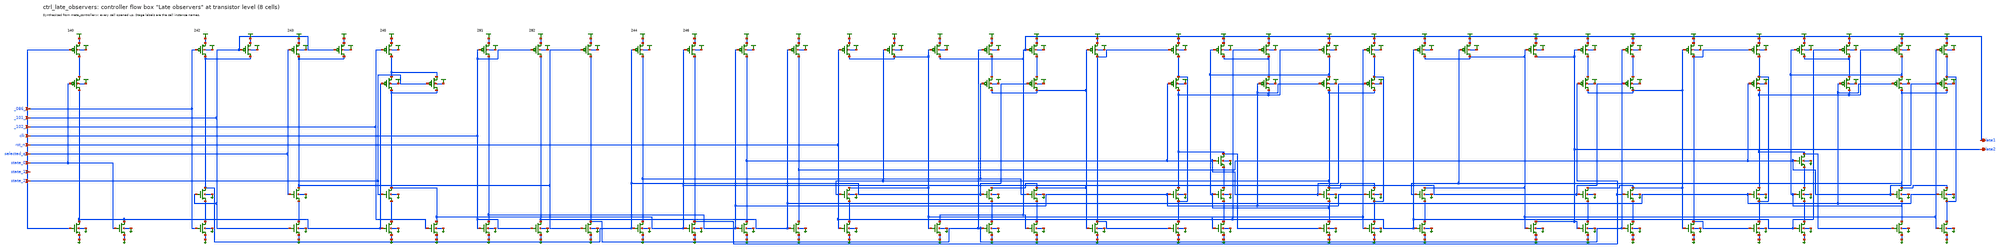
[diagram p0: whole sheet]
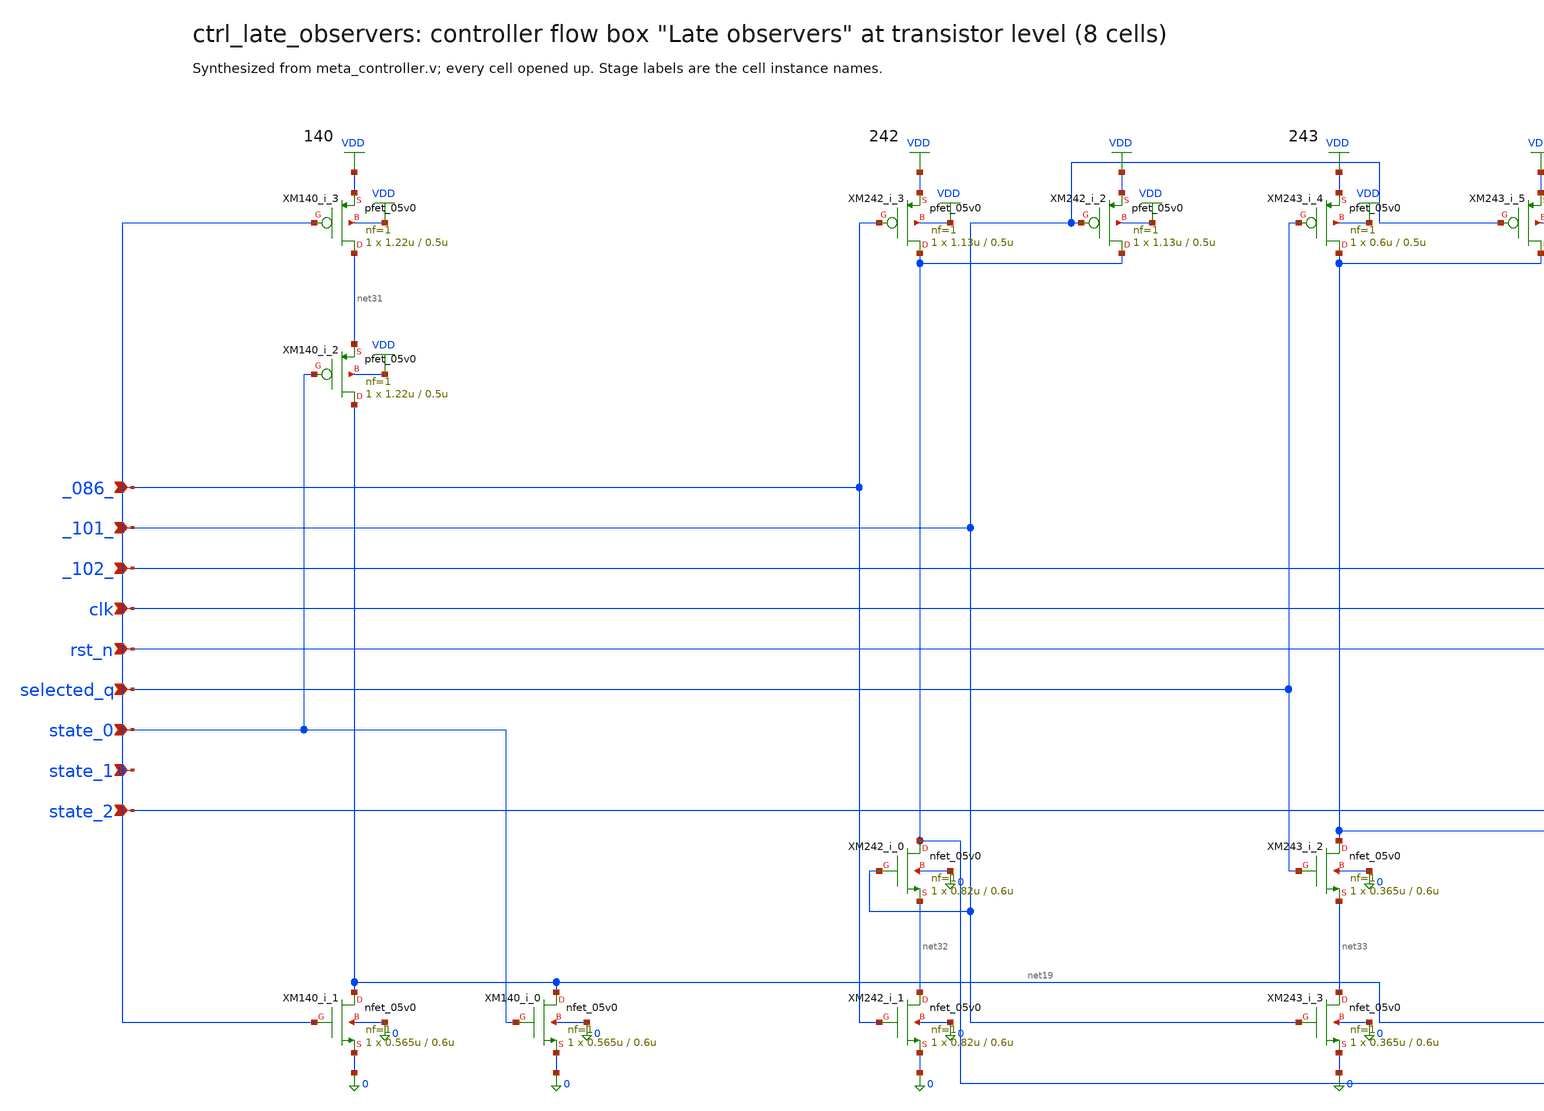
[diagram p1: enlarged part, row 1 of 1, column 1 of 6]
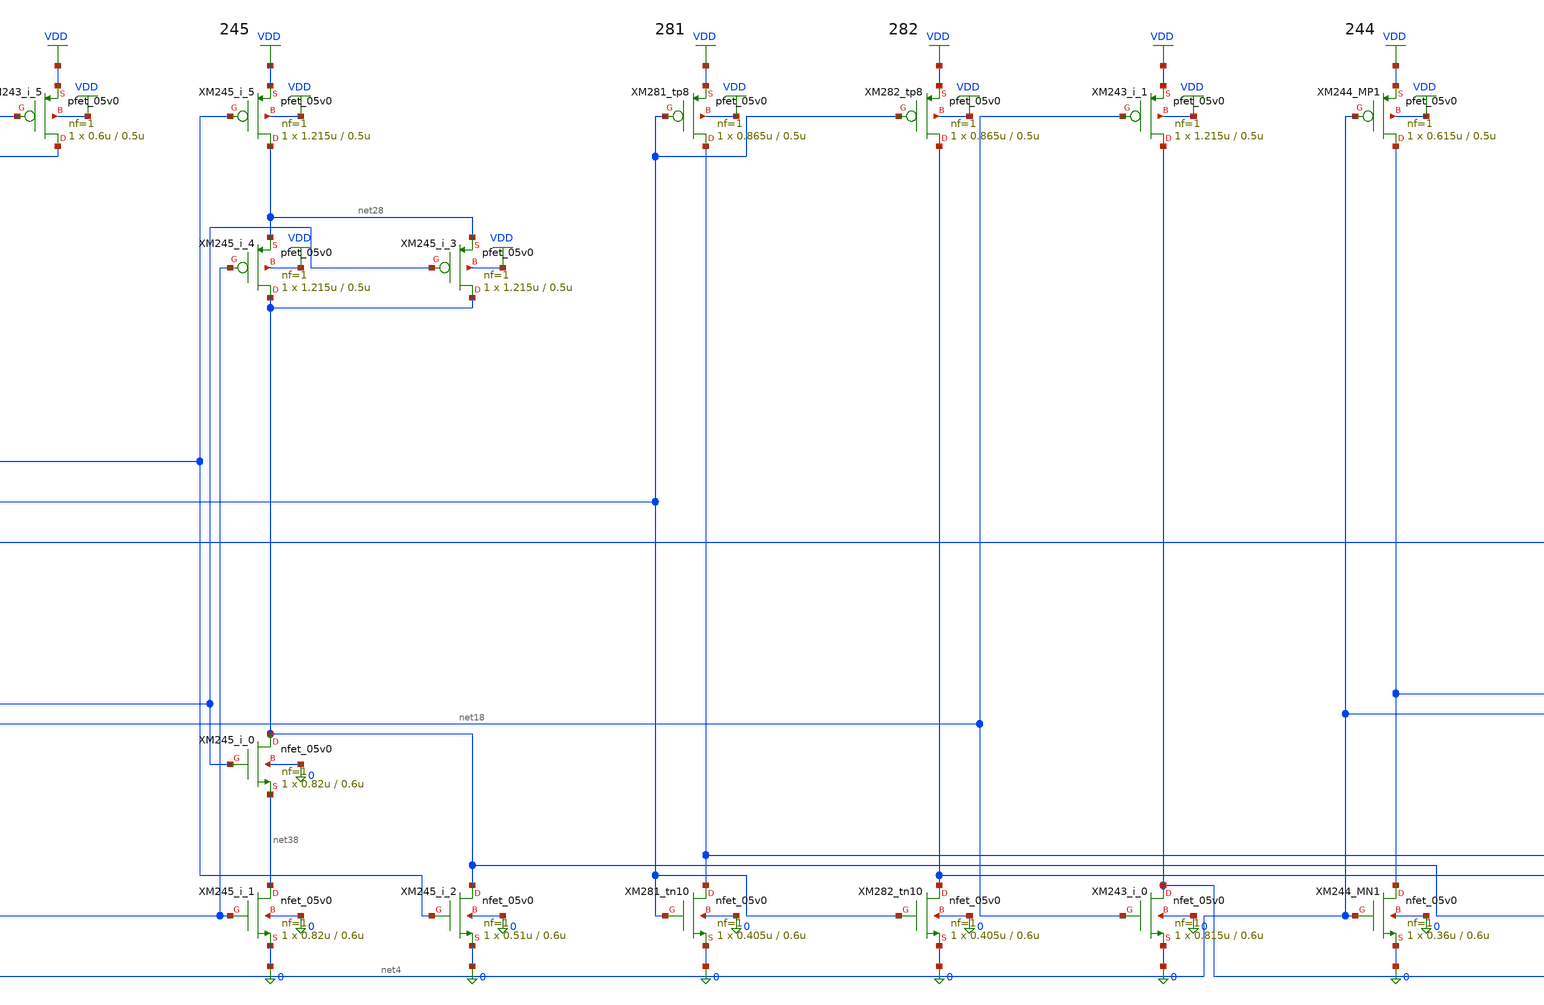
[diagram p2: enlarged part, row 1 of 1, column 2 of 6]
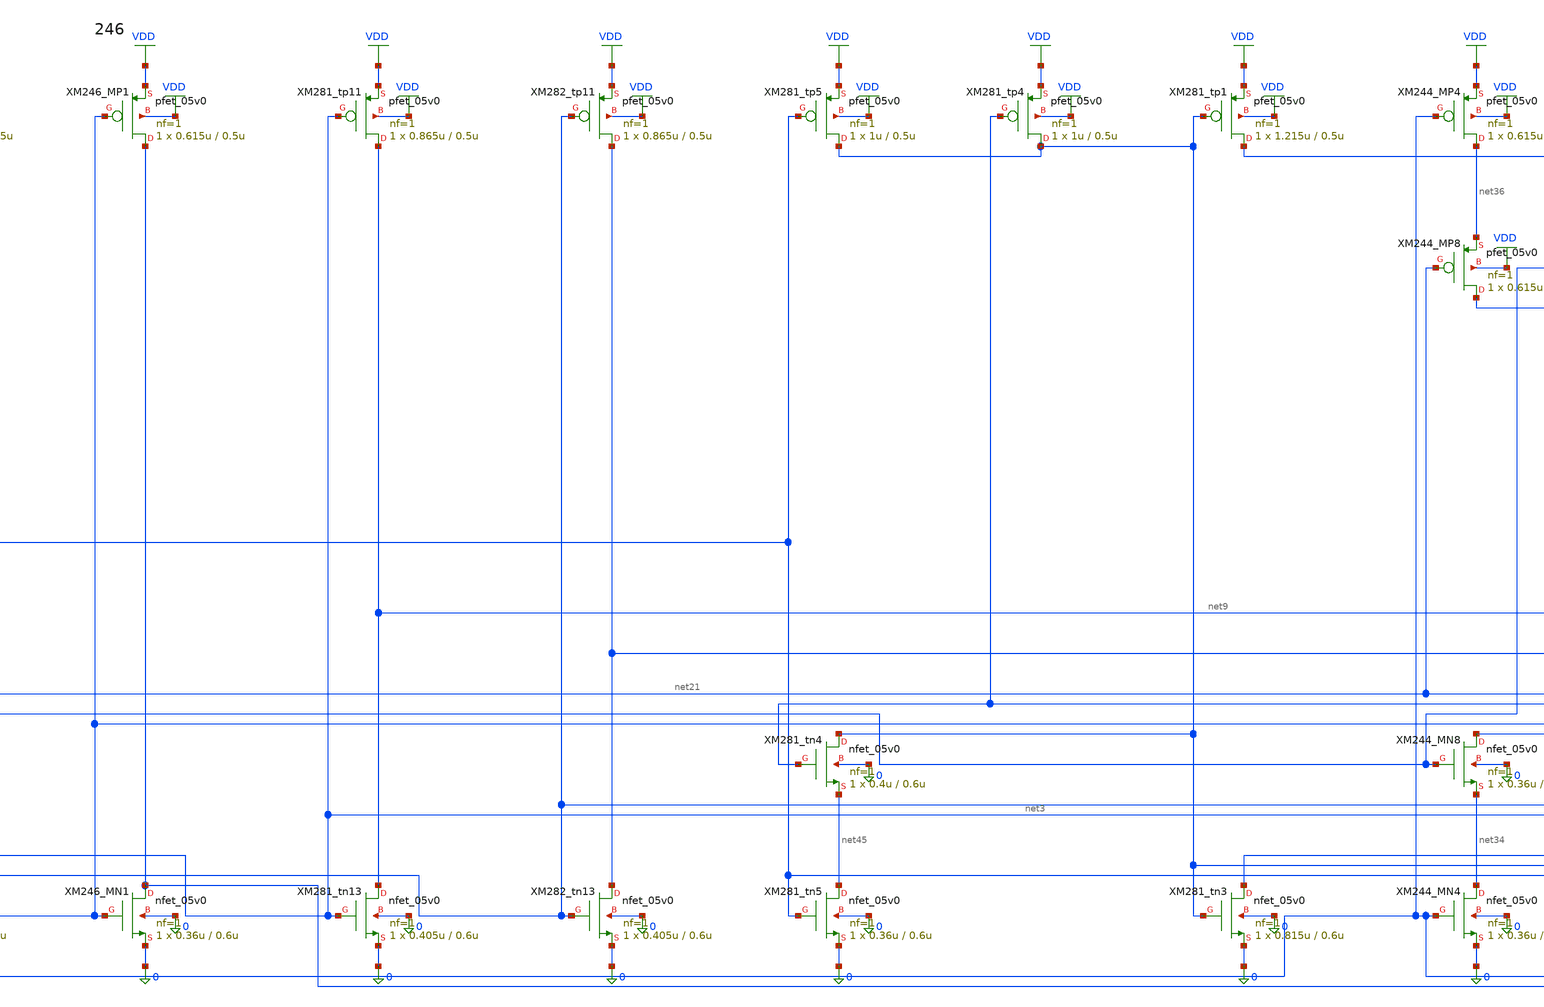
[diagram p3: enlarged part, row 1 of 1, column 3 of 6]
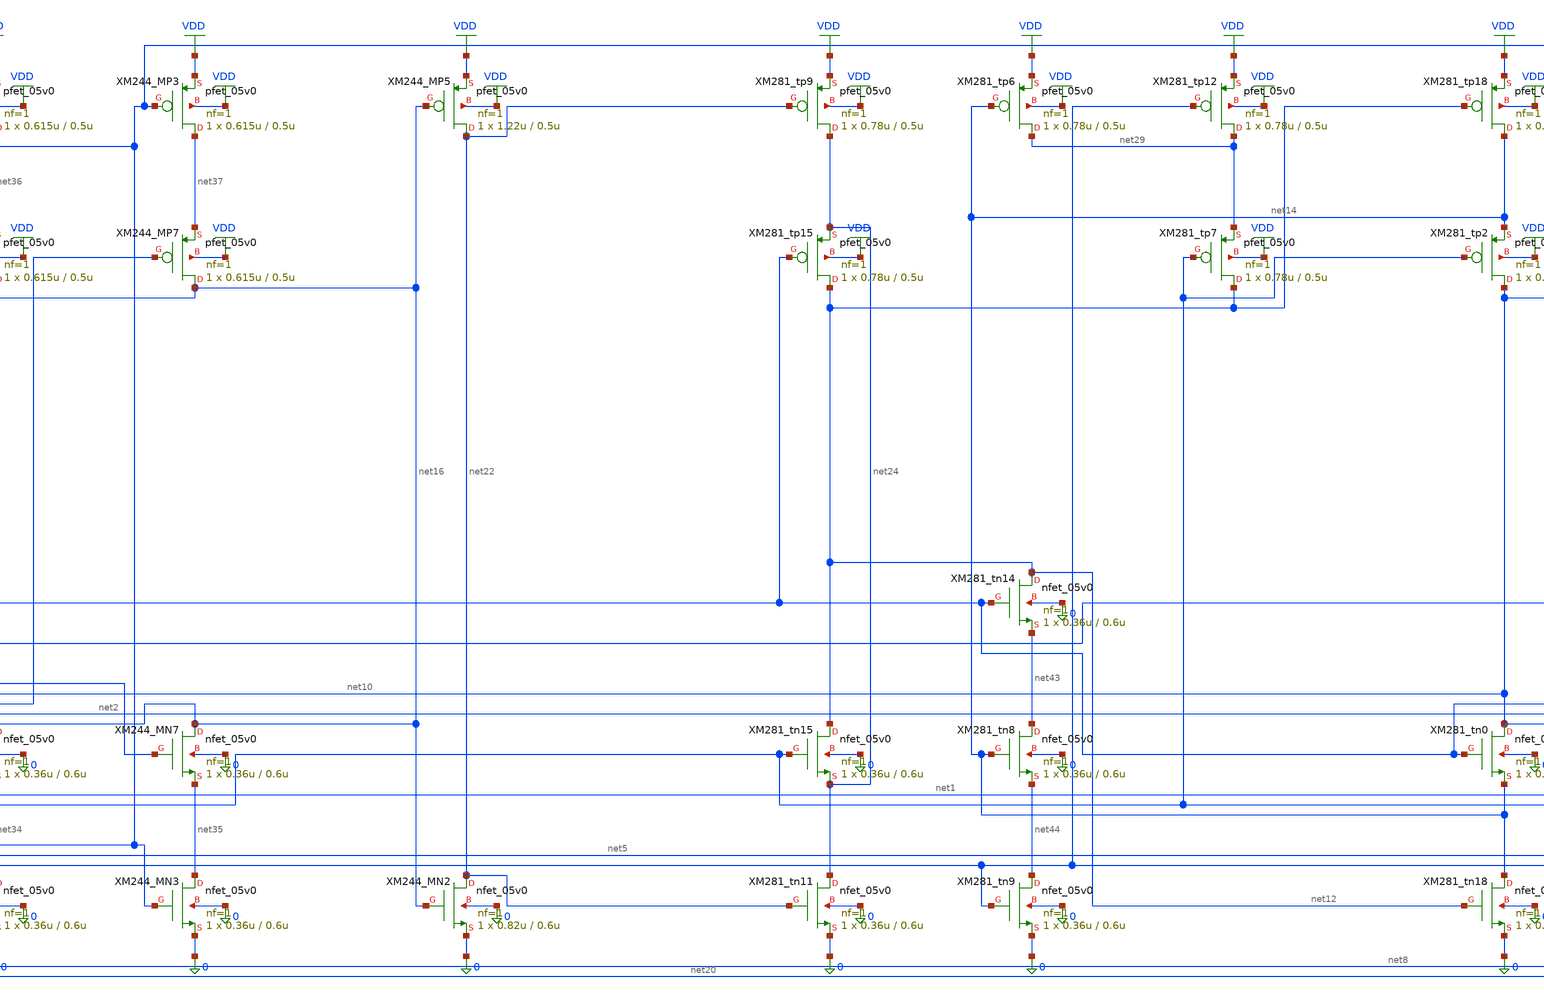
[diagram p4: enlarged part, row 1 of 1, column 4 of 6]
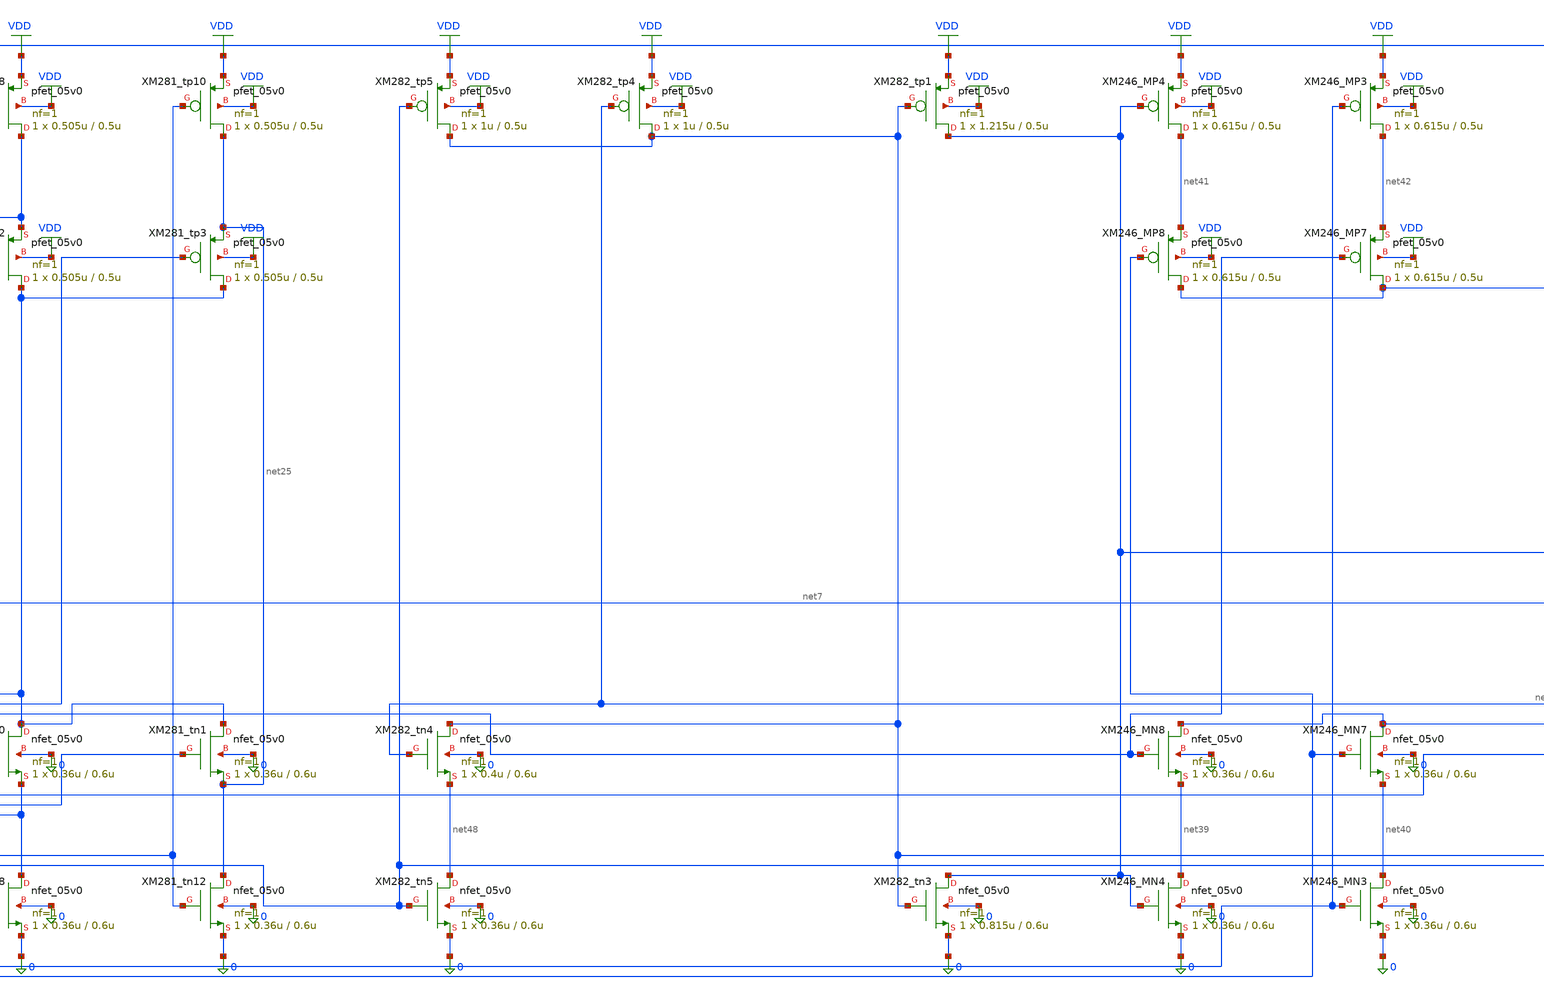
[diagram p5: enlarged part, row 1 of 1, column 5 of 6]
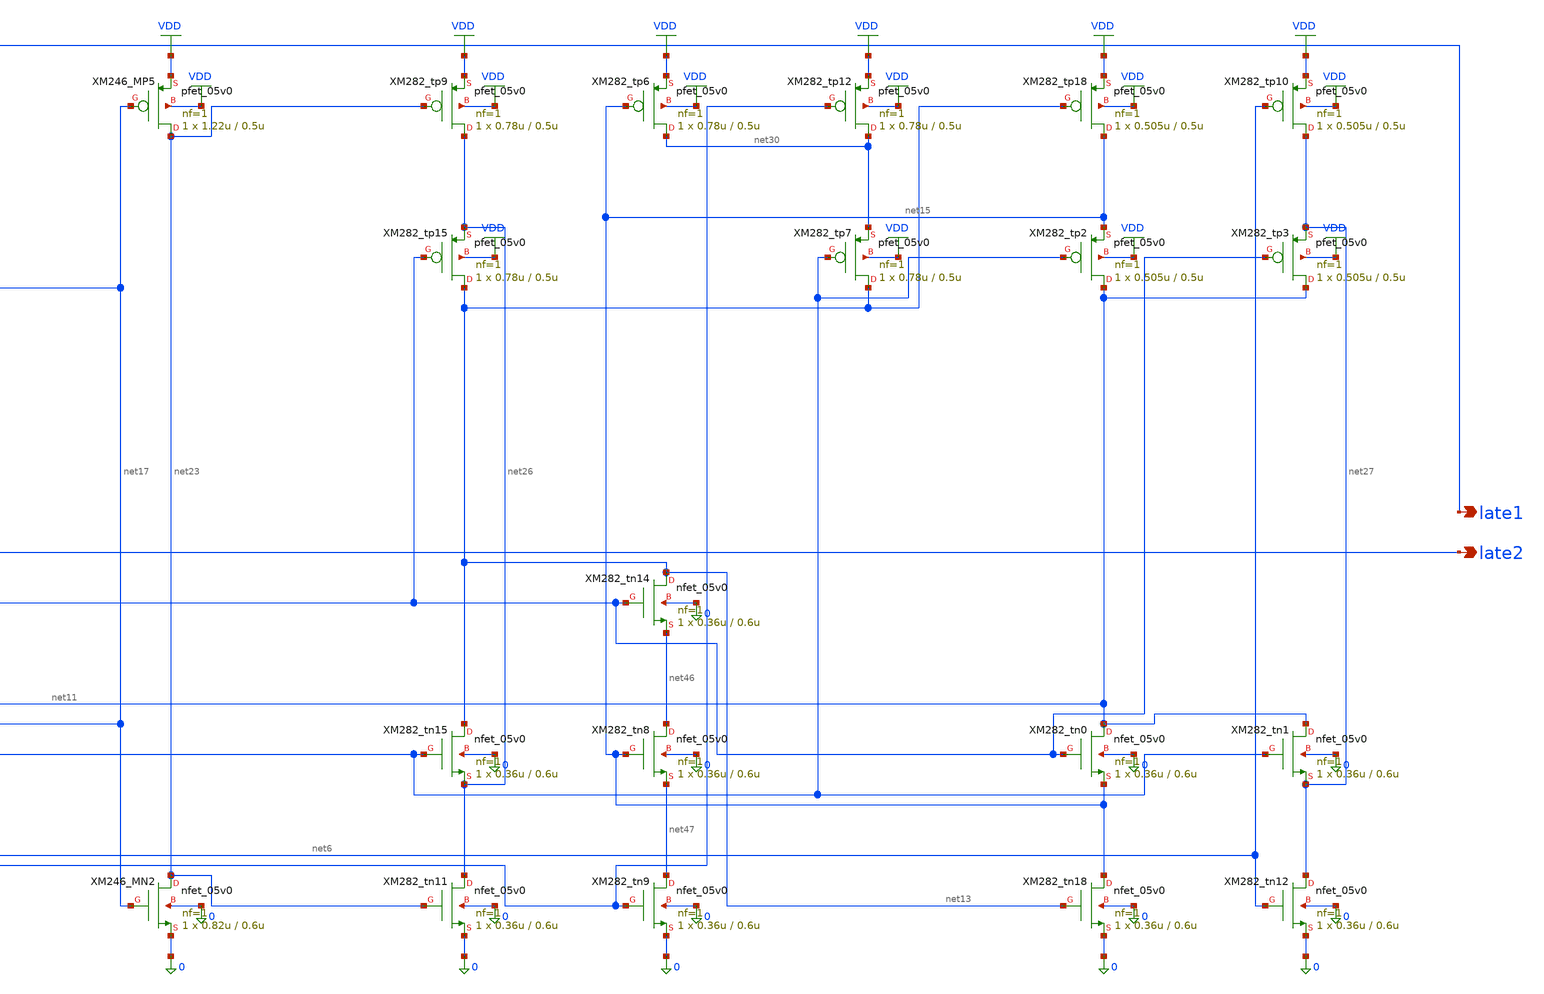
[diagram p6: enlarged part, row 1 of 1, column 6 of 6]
** sch_path: xschem/flat/ctrl_late_observers.sch
**.subckt ctrl_late_observers _086_ _101_ _102_ clk rst_n selected_q state_0 state_1 state_2 late1
*+ late2
*.ipin _086_
*.ipin _101_
*.ipin _102_
*.ipin clk
*.ipin rst_n
*.ipin selected_q
*.ipin state_0
*.ipin state_1
*.ipin state_2
*.opin late1
*.opin late2
XM140_i_1 net19 state_1 0 0 nfet_05v0 L=0.6u W=0.565u nf=1 ad=2.825e-13 as=2.825e-13 pd=2.13e-06
+ ps=2.13e-06 nrd=0 nrs=0 sa=0 sb=0 sd=0 m=1
XM140_i_0 net19 state_0 0 0 nfet_05v0 L=0.6u W=0.565u nf=1 ad=2.825e-13 as=2.825e-13 pd=2.13e-06
+ ps=2.13e-06 nrd=0 nrs=0 sa=0 sb=0 sd=0 m=1
XM140_i_3 net31 state_1 VDD VDD pfet_05v0 L=0.5u W=1.22u nf=1 ad=6.1e-13 as=6.1e-13 pd=3.44e-06
+ ps=3.44e-06 nrd=0 nrs=0 sa=0 sb=0 sd=0 m=1
XM140_i_2 net19 state_0 net31 VDD pfet_05v0 L=0.5u W=1.22u nf=1 ad=6.1e-13 as=6.1e-13 pd=3.44e-06
+ ps=3.44e-06 nrd=0 nrs=0 sa=0 sb=0 sd=0 m=1
XM242_i_1 net32 _086_ 0 0 nfet_05v0 L=0.6u W=0.82u nf=1 ad=4.1e-13 as=4.1e-13 pd=2.64e-06
+ ps=2.64e-06 nrd=0 nrs=0 sa=0 sb=0 sd=0 m=1
XM242_i_0 net4 _101_ net32 0 nfet_05v0 L=0.6u W=0.82u nf=1 ad=4.1e-13 as=4.1e-13 pd=2.64e-06
+ ps=2.64e-06 nrd=0 nrs=0 sa=0 sb=0 sd=0 m=1
XM242_i_3 net4 _086_ VDD VDD pfet_05v0 L=0.5u W=1.13u nf=1 ad=5.65e-13 as=5.65e-13 pd=3.26e-06
+ ps=3.26e-06 nrd=0 nrs=0 sa=0 sb=0 sd=0 m=1
XM242_i_2 net4 _101_ VDD VDD pfet_05v0 L=0.5u W=1.13u nf=1 ad=5.65e-13 as=5.65e-13 pd=3.26e-06
+ ps=3.26e-06 nrd=0 nrs=0 sa=0 sb=0 sd=0 m=1
XM243_i_2 net18 selected_q net33 0 nfet_05v0 L=0.6u W=0.365u nf=1 ad=1.825e-13 as=1.825e-13
+ pd=1.73e-06 ps=1.73e-06 nrd=0 nrs=0 sa=0 sb=0 sd=0 m=1
XM243_i_3 net33 _101_ 0 0 nfet_05v0 L=0.6u W=0.365u nf=1 ad=1.825e-13 as=1.825e-13 pd=1.73e-06
+ ps=1.73e-06 nrd=0 nrs=0 sa=0 sb=0 sd=0 m=1
XM243_i_0 net8 net18 0 0 nfet_05v0 L=0.6u W=0.815u nf=1 ad=4.075e-13 as=4.075e-13 pd=2.63e-06
+ ps=2.63e-06 nrd=0 nrs=0 sa=0 sb=0 sd=0 m=1
XM243_i_4 net18 selected_q VDD VDD pfet_05v0 L=0.5u W=0.6u nf=1 ad=3e-13 as=3e-13 pd=2.2e-06
+ ps=2.2e-06 nrd=0 nrs=0 sa=0 sb=0 sd=0 m=1
XM243_i_5 net18 _101_ VDD VDD pfet_05v0 L=0.5u W=0.6u nf=1 ad=3e-13 as=3e-13 pd=2.2e-06 ps=2.2e-06
+ nrd=0 nrs=0 sa=0 sb=0 sd=0 m=1
XM243_i_1 net8 net18 VDD VDD pfet_05v0 L=0.5u W=1.215u nf=1 ad=6.075e-13 as=6.075e-13 pd=3.43e-06
+ ps=3.43e-06 nrd=0 nrs=0 sa=0 sb=0 sd=0 m=1
XM244_MN2 net22 net16 0 0 nfet_05v0 L=0.6u W=0.82u nf=1 ad=4.1e-13 as=4.1e-13 pd=2.64e-06
+ ps=2.64e-06 nrd=0 nrs=0 sa=0 sb=0 sd=0 m=1
XM244_MN4 net34 net8 0 0 nfet_05v0 L=0.6u W=0.36u nf=1 ad=1.8e-13 as=1.8e-13 pd=1.72e-06 ps=1.72e-06
+ nrd=0 nrs=0 sa=0 sb=0 sd=0 m=1
XM244_MN8 net16 net4 net34 0 nfet_05v0 L=0.6u W=0.36u nf=1 ad=1.8e-13 as=1.8e-13 pd=1.72e-06
+ ps=1.72e-06 nrd=0 nrs=0 sa=0 sb=0 sd=0 m=1
XM244_MN7 net16 net21 net35 0 nfet_05v0 L=0.6u W=0.36u nf=1 ad=1.8e-13 as=1.8e-13 pd=1.72e-06
+ ps=1.72e-06 nrd=0 nrs=0 sa=0 sb=0 sd=0 m=1
XM244_MN3 net35 late1 0 0 nfet_05v0 L=0.6u W=0.36u nf=1 ad=1.8e-13 as=1.8e-13 pd=1.72e-06
+ ps=1.72e-06 nrd=0 nrs=0 sa=0 sb=0 sd=0 m=1
XM244_MN1 net21 net4 0 0 nfet_05v0 L=0.6u W=0.36u nf=1 ad=1.8e-13 as=1.8e-13 pd=1.72e-06 ps=1.72e-06
+ nrd=0 nrs=0 sa=0 sb=0 sd=0 m=1
XM244_MP5 net22 net16 VDD VDD pfet_05v0 L=0.5u W=1.22u nf=1 ad=6.1e-13 as=6.1e-13 pd=3.44e-06
+ ps=3.44e-06 nrd=0 nrs=0 sa=0 sb=0 sd=0 m=1
XM244_MP4 net36 net8 VDD VDD pfet_05v0 L=0.5u W=0.615u nf=1 ad=3.075e-13 as=3.075e-13 pd=2.23e-06
+ ps=2.23e-06 nrd=0 nrs=0 sa=0 sb=0 sd=0 m=1
XM244_MP8 net16 net21 net36 VDD pfet_05v0 L=0.5u W=0.615u nf=1 ad=3.075e-13 as=3.075e-13 pd=2.23e-06
+ ps=2.23e-06 nrd=0 nrs=0 sa=0 sb=0 sd=0 m=1
XM244_MP7 net16 net4 net37 VDD pfet_05v0 L=0.5u W=0.615u nf=1 ad=3.075e-13 as=3.075e-13 pd=2.23e-06
+ ps=2.23e-06 nrd=0 nrs=0 sa=0 sb=0 sd=0 m=1
XM244_MP3 net37 late1 VDD VDD pfet_05v0 L=0.5u W=0.615u nf=1 ad=3.075e-13 as=3.075e-13 pd=2.23e-06
+ ps=2.23e-06 nrd=0 nrs=0 sa=0 sb=0 sd=0 m=1
XM244_MP1 net21 net4 VDD VDD pfet_05v0 L=0.5u W=0.615u nf=1 ad=3.075e-13 as=3.075e-13 pd=2.23e-06
+ ps=2.23e-06 nrd=0 nrs=0 sa=0 sb=0 sd=0 m=1
XM245_i_1 net38 net19 0 0 nfet_05v0 L=0.6u W=0.82u nf=1 ad=4.1e-13 as=4.1e-13 pd=2.64e-06
+ ps=2.64e-06 nrd=0 nrs=0 sa=0 sb=0 sd=0 m=1
XM245_i_0 net2 state_2 net38 0 nfet_05v0 L=0.6u W=0.82u nf=1 ad=4.1e-13 as=4.1e-13 pd=2.64e-06
+ ps=2.64e-06 nrd=0 nrs=0 sa=0 sb=0 sd=0 m=1
XM245_i_2 net2 _102_ 0 0 nfet_05v0 L=0.6u W=0.51u nf=1 ad=2.55e-13 as=2.55e-13 pd=2.02e-06
+ ps=2.02e-06 nrd=0 nrs=0 sa=0 sb=0 sd=0 m=1
XM245_i_4 net2 net19 net28 VDD pfet_05v0 L=0.5u W=1.215u nf=1 ad=6.075e-13 as=6.075e-13 pd=3.43e-06
+ ps=3.43e-06 nrd=0 nrs=0 sa=0 sb=0 sd=0 m=1
XM245_i_3 net2 state_2 net28 VDD pfet_05v0 L=0.5u W=1.215u nf=1 ad=6.075e-13 as=6.075e-13
+ pd=3.43e-06 ps=3.43e-06 nrd=0 nrs=0 sa=0 sb=0 sd=0 m=1
XM245_i_5 net28 _102_ VDD VDD pfet_05v0 L=0.5u W=1.215u nf=1 ad=6.075e-13 as=6.075e-13 pd=3.43e-06
+ ps=3.43e-06 nrd=0 nrs=0 sa=0 sb=0 sd=0 m=1
XM246_MN2 net23 net17 0 0 nfet_05v0 L=0.6u W=0.82u nf=1 ad=4.1e-13 as=4.1e-13 pd=2.64e-06
+ ps=2.64e-06 nrd=0 nrs=0 sa=0 sb=0 sd=0 m=1
XM246_MN4 net39 late2 0 0 nfet_05v0 L=0.6u W=0.36u nf=1 ad=1.8e-13 as=1.8e-13 pd=1.72e-06
+ ps=1.72e-06 nrd=0 nrs=0 sa=0 sb=0 sd=0 m=1
XM246_MN8 net17 net2 net39 0 nfet_05v0 L=0.6u W=0.36u nf=1 ad=1.8e-13 as=1.8e-13 pd=1.72e-06
+ ps=1.72e-06 nrd=0 nrs=0 sa=0 sb=0 sd=0 m=1
XM246_MN7 net17 net20 net40 0 nfet_05v0 L=0.6u W=0.36u nf=1 ad=1.8e-13 as=1.8e-13 pd=1.72e-06
+ ps=1.72e-06 nrd=0 nrs=0 sa=0 sb=0 sd=0 m=1
XM246_MN3 net40 net8 0 0 nfet_05v0 L=0.6u W=0.36u nf=1 ad=1.8e-13 as=1.8e-13 pd=1.72e-06 ps=1.72e-06
+ nrd=0 nrs=0 sa=0 sb=0 sd=0 m=1
XM246_MN1 net20 net2 0 0 nfet_05v0 L=0.6u W=0.36u nf=1 ad=1.8e-13 as=1.8e-13 pd=1.72e-06 ps=1.72e-06
+ nrd=0 nrs=0 sa=0 sb=0 sd=0 m=1
XM246_MP5 net23 net17 VDD VDD pfet_05v0 L=0.5u W=1.22u nf=1 ad=6.1e-13 as=6.1e-13 pd=3.44e-06
+ ps=3.44e-06 nrd=0 nrs=0 sa=0 sb=0 sd=0 m=1
XM246_MP4 net41 late2 VDD VDD pfet_05v0 L=0.5u W=0.615u nf=1 ad=3.075e-13 as=3.075e-13 pd=2.23e-06
+ ps=2.23e-06 nrd=0 nrs=0 sa=0 sb=0 sd=0 m=1
XM246_MP8 net17 net20 net41 VDD pfet_05v0 L=0.5u W=0.615u nf=1 ad=3.075e-13 as=3.075e-13 pd=2.23e-06
+ ps=2.23e-06 nrd=0 nrs=0 sa=0 sb=0 sd=0 m=1
XM246_MP7 net17 net2 net42 VDD pfet_05v0 L=0.5u W=0.615u nf=1 ad=3.075e-13 as=3.075e-13 pd=2.23e-06
+ ps=2.23e-06 nrd=0 nrs=0 sa=0 sb=0 sd=0 m=1
XM246_MP3 net42 net8 VDD VDD pfet_05v0 L=0.5u W=0.615u nf=1 ad=3.075e-13 as=3.075e-13 pd=2.23e-06
+ ps=2.23e-06 nrd=0 nrs=0 sa=0 sb=0 sd=0 m=1
XM246_MP1 net20 net2 VDD VDD pfet_05v0 L=0.5u W=0.615u nf=1 ad=3.075e-13 as=3.075e-13 pd=2.23e-06
+ ps=2.23e-06 nrd=0 nrs=0 sa=0 sb=0 sd=0 m=1
XM281_tn10 net3 clk 0 0 nfet_05v0 L=0.6u W=0.405u nf=1 ad=2.025e-13 as=2.025e-13 pd=1.81e-06
+ ps=1.81e-06 nrd=0 nrs=0 sa=0 sb=0 sd=0 m=1
XM281_tn13 net9 net3 0 0 nfet_05v0 L=0.6u W=0.405u nf=1 ad=2.025e-13 as=2.025e-13 pd=1.81e-06
+ ps=1.81e-06 nrd=0 nrs=0 sa=0 sb=0 sd=0 m=1
XM281_tn11 net24 net22 0 0 nfet_05v0 L=0.6u W=0.36u nf=1 ad=1.8e-13 as=1.8e-13 pd=1.72e-06
+ ps=1.72e-06 nrd=0 nrs=0 sa=0 sb=0 sd=0 m=1
XM281_tn15 net12 net3 net24 0 nfet_05v0 L=0.6u W=0.36u nf=1 ad=1.8e-13 as=1.8e-13 pd=1.72e-06
+ ps=1.72e-06 nrd=0 nrs=0 sa=0 sb=0 sd=0 m=1
XM281_tn14 net12 net9 net43 0 nfet_05v0 L=0.6u W=0.36u nf=1 ad=1.8e-13 as=1.8e-13 pd=1.72e-06
+ ps=1.72e-06 nrd=0 nrs=0 sa=0 sb=0 sd=0 m=1
XM281_tn8 net43 net14 net44 0 nfet_05v0 L=0.6u W=0.36u nf=1 ad=1.8e-13 as=1.8e-13 pd=1.72e-06
+ ps=1.72e-06 nrd=0 nrs=0 sa=0 sb=0 sd=0 m=1
XM281_tn9 net44 rst_n 0 0 nfet_05v0 L=0.6u W=0.36u nf=1 ad=1.8e-13 as=1.8e-13 pd=1.72e-06
+ ps=1.72e-06 nrd=0 nrs=0 sa=0 sb=0 sd=0 m=1
XM281_tn18 net14 net12 0 0 nfet_05v0 L=0.6u W=0.36u nf=1 ad=1.8e-13 as=1.8e-13 pd=1.72e-06
+ ps=1.72e-06 nrd=0 nrs=0 sa=0 sb=0 sd=0 m=1
XM281_tn0 net10 net9 net14 0 nfet_05v0 L=0.6u W=0.36u nf=1 ad=1.8e-13 as=1.8e-13 pd=1.72e-06
+ ps=1.72e-06 nrd=0 nrs=0 sa=0 sb=0 sd=0 m=1
XM281_tn1 net10 net3 net25 0 nfet_05v0 L=0.6u W=0.36u nf=1 ad=1.8e-13 as=1.8e-13 pd=1.72e-06
+ ps=1.72e-06 nrd=0 nrs=0 sa=0 sb=0 sd=0 m=1
XM281_tn12 net25 net5 0 0 nfet_05v0 L=0.6u W=0.36u nf=1 ad=1.8e-13 as=1.8e-13 pd=1.72e-06
+ ps=1.72e-06 nrd=0 nrs=0 sa=0 sb=0 sd=0 m=1
XM281_tn5 net45 rst_n 0 0 nfet_05v0 L=0.6u W=0.36u nf=1 ad=1.8e-13 as=1.8e-13 pd=1.72e-06
+ ps=1.72e-06 nrd=0 nrs=0 sa=0 sb=0 sd=0 m=1
XM281_tn4 net5 net10 net45 0 nfet_05v0 L=0.6u W=0.4u nf=1 ad=2e-13 as=2e-13 pd=1.8e-06 ps=1.8e-06
+ nrd=0 nrs=0 sa=0 sb=0 sd=0 m=1
XM281_tn3 late1 net5 0 0 nfet_05v0 L=0.6u W=0.815u nf=1 ad=4.075e-13 as=4.075e-13 pd=2.63e-06
+ ps=2.63e-06 nrd=0 nrs=0 sa=0 sb=0 sd=0 m=1
XM281_tp8 net3 clk VDD VDD pfet_05v0 L=0.5u W=0.865u nf=1 ad=4.325e-13 as=4.325e-13 pd=2.73e-06
+ ps=2.73e-06 nrd=0 nrs=0 sa=0 sb=0 sd=0 m=1
XM281_tp11 net9 net3 VDD VDD pfet_05v0 L=0.5u W=0.865u nf=1 ad=4.325e-13 as=4.325e-13 pd=2.73e-06
+ ps=2.73e-06 nrd=0 nrs=0 sa=0 sb=0 sd=0 m=1
XM281_tp9 net24 net22 VDD VDD pfet_05v0 L=0.5u W=0.78u nf=1 ad=3.9e-13 as=3.9e-13 pd=2.56e-06
+ ps=2.56e-06 nrd=0 nrs=0 sa=0 sb=0 sd=0 m=1
XM281_tp15 net12 net9 net24 VDD pfet_05v0 L=0.5u W=0.78u nf=1 ad=3.9e-13 as=3.9e-13 pd=2.56e-06
+ ps=2.56e-06 nrd=0 nrs=0 sa=0 sb=0 sd=0 m=1
XM281_tp7 net12 net3 net29 VDD pfet_05v0 L=0.5u W=0.78u nf=1 ad=3.9e-13 as=3.9e-13 pd=2.56e-06
+ ps=2.56e-06 nrd=0 nrs=0 sa=0 sb=0 sd=0 m=1
XM281_tp6 net29 net14 VDD VDD pfet_05v0 L=0.5u W=0.78u nf=1 ad=3.9e-13 as=3.9e-13 pd=2.56e-06
+ ps=2.56e-06 nrd=0 nrs=0 sa=0 sb=0 sd=0 m=1
XM281_tp12 net29 rst_n VDD VDD pfet_05v0 L=0.5u W=0.78u nf=1 ad=3.9e-13 as=3.9e-13 pd=2.56e-06
+ ps=2.56e-06 nrd=0 nrs=0 sa=0 sb=0 sd=0 m=1
XM281_tp18 net14 net12 VDD VDD pfet_05v0 L=0.5u W=0.505u nf=1 ad=2.525e-13 as=2.525e-13 pd=2.01e-06
+ ps=2.01e-06 nrd=0 nrs=0 sa=0 sb=0 sd=0 m=1
XM281_tp2 net10 net3 net14 VDD pfet_05v0 L=0.5u W=0.505u nf=1 ad=2.525e-13 as=2.525e-13 pd=2.01e-06
+ ps=2.01e-06 nrd=0 nrs=0 sa=0 sb=0 sd=0 m=1
XM281_tp3 net10 net9 net25 VDD pfet_05v0 L=0.5u W=0.505u nf=1 ad=2.525e-13 as=2.525e-13 pd=2.01e-06
+ ps=2.01e-06 nrd=0 nrs=0 sa=0 sb=0 sd=0 m=1
XM281_tp10 net25 net5 VDD VDD pfet_05v0 L=0.5u W=0.505u nf=1 ad=2.525e-13 as=2.525e-13 pd=2.01e-06
+ ps=2.01e-06 nrd=0 nrs=0 sa=0 sb=0 sd=0 m=1
XM281_tp5 net5 rst_n VDD VDD pfet_05v0 L=0.5u W=1u nf=1 ad=5e-13 as=5e-13 pd=3e-06 ps=3e-06 nrd=0
+ nrs=0 sa=0 sb=0 sd=0 m=1
XM281_tp4 net5 net10 VDD VDD pfet_05v0 L=0.5u W=1u nf=1 ad=5e-13 as=5e-13 pd=3e-06 ps=3e-06 nrd=0
+ nrs=0 sa=0 sb=0 sd=0 m=1
XM281_tp1 late1 net5 VDD VDD pfet_05v0 L=0.5u W=1.215u nf=1 ad=6.075e-13 as=6.075e-13 pd=3.43e-06
+ ps=3.43e-06 nrd=0 nrs=0 sa=0 sb=0 sd=0 m=1
XM282_tn10 net1 clk 0 0 nfet_05v0 L=0.6u W=0.405u nf=1 ad=2.025e-13 as=2.025e-13 pd=1.81e-06
+ ps=1.81e-06 nrd=0 nrs=0 sa=0 sb=0 sd=0 m=1
XM282_tn13 net7 net1 0 0 nfet_05v0 L=0.6u W=0.405u nf=1 ad=2.025e-13 as=2.025e-13 pd=1.81e-06
+ ps=1.81e-06 nrd=0 nrs=0 sa=0 sb=0 sd=0 m=1
XM282_tn11 net26 net23 0 0 nfet_05v0 L=0.6u W=0.36u nf=1 ad=1.8e-13 as=1.8e-13 pd=1.72e-06
+ ps=1.72e-06 nrd=0 nrs=0 sa=0 sb=0 sd=0 m=1
XM282_tn15 net13 net1 net26 0 nfet_05v0 L=0.6u W=0.36u nf=1 ad=1.8e-13 as=1.8e-13 pd=1.72e-06
+ ps=1.72e-06 nrd=0 nrs=0 sa=0 sb=0 sd=0 m=1
XM282_tn14 net13 net7 net46 0 nfet_05v0 L=0.6u W=0.36u nf=1 ad=1.8e-13 as=1.8e-13 pd=1.72e-06
+ ps=1.72e-06 nrd=0 nrs=0 sa=0 sb=0 sd=0 m=1
XM282_tn8 net46 net15 net47 0 nfet_05v0 L=0.6u W=0.36u nf=1 ad=1.8e-13 as=1.8e-13 pd=1.72e-06
+ ps=1.72e-06 nrd=0 nrs=0 sa=0 sb=0 sd=0 m=1
XM282_tn9 net47 rst_n 0 0 nfet_05v0 L=0.6u W=0.36u nf=1 ad=1.8e-13 as=1.8e-13 pd=1.72e-06
+ ps=1.72e-06 nrd=0 nrs=0 sa=0 sb=0 sd=0 m=1
XM282_tn18 net15 net13 0 0 nfet_05v0 L=0.6u W=0.36u nf=1 ad=1.8e-13 as=1.8e-13 pd=1.72e-06
+ ps=1.72e-06 nrd=0 nrs=0 sa=0 sb=0 sd=0 m=1
XM282_tn0 net11 net7 net15 0 nfet_05v0 L=0.6u W=0.36u nf=1 ad=1.8e-13 as=1.8e-13 pd=1.72e-06
+ ps=1.72e-06 nrd=0 nrs=0 sa=0 sb=0 sd=0 m=1
XM282_tn1 net11 net1 net27 0 nfet_05v0 L=0.6u W=0.36u nf=1 ad=1.8e-13 as=1.8e-13 pd=1.72e-06
+ ps=1.72e-06 nrd=0 nrs=0 sa=0 sb=0 sd=0 m=1
XM282_tn12 net27 net6 0 0 nfet_05v0 L=0.6u W=0.36u nf=1 ad=1.8e-13 as=1.8e-13 pd=1.72e-06
+ ps=1.72e-06 nrd=0 nrs=0 sa=0 sb=0 sd=0 m=1
XM282_tn5 net48 rst_n 0 0 nfet_05v0 L=0.6u W=0.36u nf=1 ad=1.8e-13 as=1.8e-13 pd=1.72e-06
+ ps=1.72e-06 nrd=0 nrs=0 sa=0 sb=0 sd=0 m=1
XM282_tn4 net6 net11 net48 0 nfet_05v0 L=0.6u W=0.4u nf=1 ad=2e-13 as=2e-13 pd=1.8e-06 ps=1.8e-06
+ nrd=0 nrs=0 sa=0 sb=0 sd=0 m=1
XM282_tn3 late2 net6 0 0 nfet_05v0 L=0.6u W=0.815u nf=1 ad=4.075e-13 as=4.075e-13 pd=2.63e-06
+ ps=2.63e-06 nrd=0 nrs=0 sa=0 sb=0 sd=0 m=1
XM282_tp8 net1 clk VDD VDD pfet_05v0 L=0.5u W=0.865u nf=1 ad=4.325e-13 as=4.325e-13 pd=2.73e-06
+ ps=2.73e-06 nrd=0 nrs=0 sa=0 sb=0 sd=0 m=1
XM282_tp11 net7 net1 VDD VDD pfet_05v0 L=0.5u W=0.865u nf=1 ad=4.325e-13 as=4.325e-13 pd=2.73e-06
+ ps=2.73e-06 nrd=0 nrs=0 sa=0 sb=0 sd=0 m=1
XM282_tp9 net26 net23 VDD VDD pfet_05v0 L=0.5u W=0.78u nf=1 ad=3.9e-13 as=3.9e-13 pd=2.56e-06
+ ps=2.56e-06 nrd=0 nrs=0 sa=0 sb=0 sd=0 m=1
XM282_tp15 net13 net7 net26 VDD pfet_05v0 L=0.5u W=0.78u nf=1 ad=3.9e-13 as=3.9e-13 pd=2.56e-06
+ ps=2.56e-06 nrd=0 nrs=0 sa=0 sb=0 sd=0 m=1
XM282_tp7 net13 net1 net30 VDD pfet_05v0 L=0.5u W=0.78u nf=1 ad=3.9e-13 as=3.9e-13 pd=2.56e-06
+ ps=2.56e-06 nrd=0 nrs=0 sa=0 sb=0 sd=0 m=1
XM282_tp6 net30 net15 VDD VDD pfet_05v0 L=0.5u W=0.78u nf=1 ad=3.9e-13 as=3.9e-13 pd=2.56e-06
+ ps=2.56e-06 nrd=0 nrs=0 sa=0 sb=0 sd=0 m=1
XM282_tp12 net30 rst_n VDD VDD pfet_05v0 L=0.5u W=0.78u nf=1 ad=3.9e-13 as=3.9e-13 pd=2.56e-06
+ ps=2.56e-06 nrd=0 nrs=0 sa=0 sb=0 sd=0 m=1
XM282_tp18 net15 net13 VDD VDD pfet_05v0 L=0.5u W=0.505u nf=1 ad=2.525e-13 as=2.525e-13 pd=2.01e-06
+ ps=2.01e-06 nrd=0 nrs=0 sa=0 sb=0 sd=0 m=1
XM282_tp2 net11 net1 net15 VDD pfet_05v0 L=0.5u W=0.505u nf=1 ad=2.525e-13 as=2.525e-13 pd=2.01e-06
+ ps=2.01e-06 nrd=0 nrs=0 sa=0 sb=0 sd=0 m=1
XM282_tp3 net11 net7 net27 VDD pfet_05v0 L=0.5u W=0.505u nf=1 ad=2.525e-13 as=2.525e-13 pd=2.01e-06
+ ps=2.01e-06 nrd=0 nrs=0 sa=0 sb=0 sd=0 m=1
XM282_tp10 net27 net6 VDD VDD pfet_05v0 L=0.5u W=0.505u nf=1 ad=2.525e-13 as=2.525e-13 pd=2.01e-06
+ ps=2.01e-06 nrd=0 nrs=0 sa=0 sb=0 sd=0 m=1
XM282_tp5 net6 rst_n VDD VDD pfet_05v0 L=0.5u W=1u nf=1 ad=5e-13 as=5e-13 pd=3e-06 ps=3e-06 nrd=0
+ nrs=0 sa=0 sb=0 sd=0 m=1
XM282_tp4 net6 net11 VDD VDD pfet_05v0 L=0.5u W=1u nf=1 ad=5e-13 as=5e-13 pd=3e-06 ps=3e-06 nrd=0
+ nrs=0 sa=0 sb=0 sd=0 m=1
XM282_tp1 late2 net6 VDD VDD pfet_05v0 L=0.5u W=1.215u nf=1 ad=6.075e-13 as=6.075e-13 pd=3.43e-06
+ ps=3.43e-06 nrd=0 nrs=0 sa=0 sb=0 sd=0 m=1
**.ends
.GLOBAL VDD
.end
